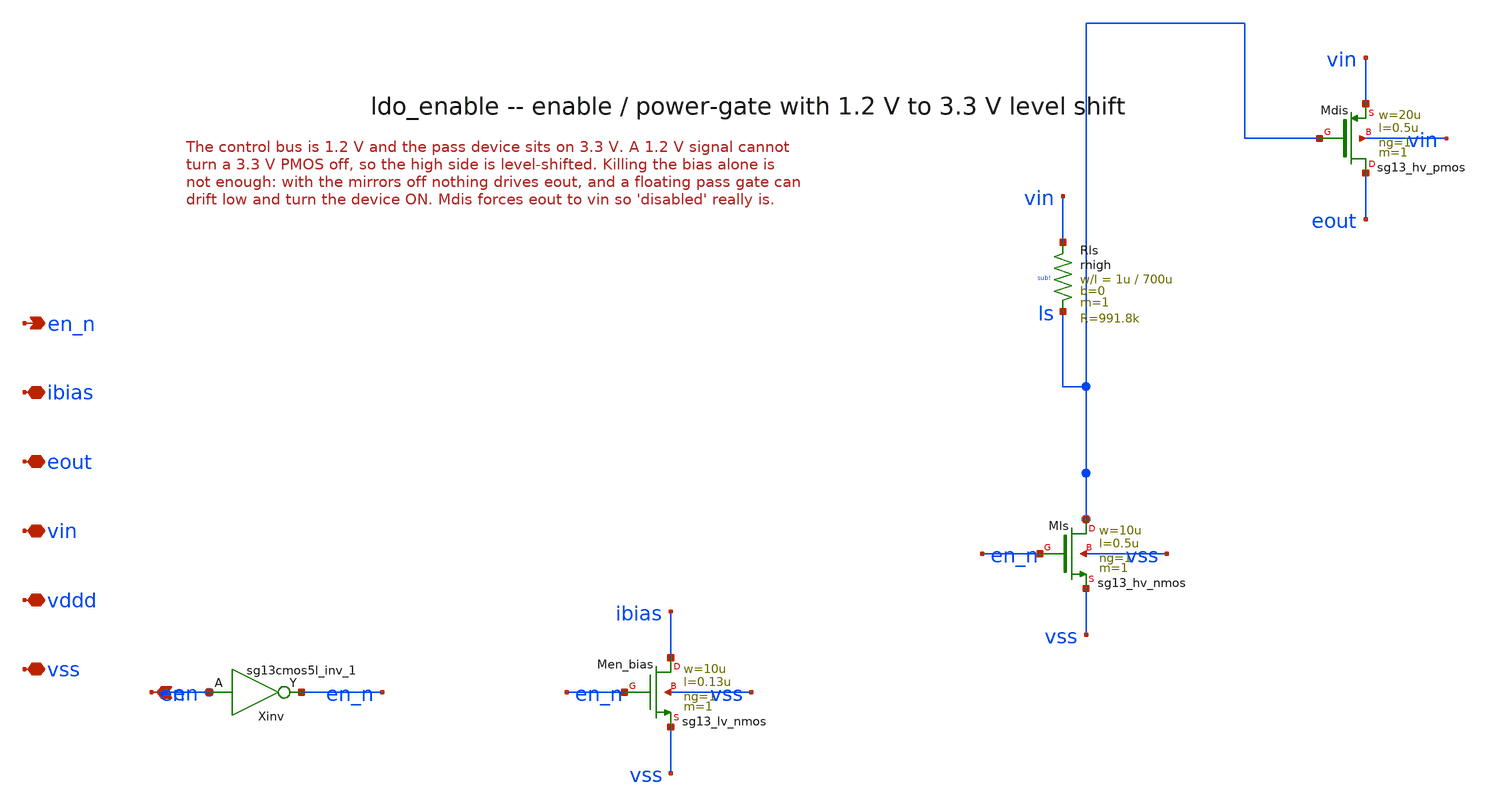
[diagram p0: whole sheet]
** sch_path: xschem/ldo_enable.sch
**.subckt ldo_enable en en_n ibias eout vin vddd vss
*.ipin en
*.opin en_n
*.iopin ibias
*.iopin eout
*.iopin vin
*.iopin vddd
*.iopin vss
Xinv en_n en vddd vss sg13cmos5l_inv_1
XMen_bias ibias en_n vss vss sg13_lv_nmos w=10u l=0.13u ng=1 m=1 mm_ok=1
XRls vin ls sub! rhigh w=1u l=700u m=1 b=0 mm_ok=1
XMls ls en_n vss vss sg13_hv_nmos w=10u l=0.5u ng=1 m=1 mm_ok=1
XMdis eout ls vin vin sg13_hv_pmos w=20u l=0.5u ng=1 m=1 mm_ok=1
**.ends
.end
